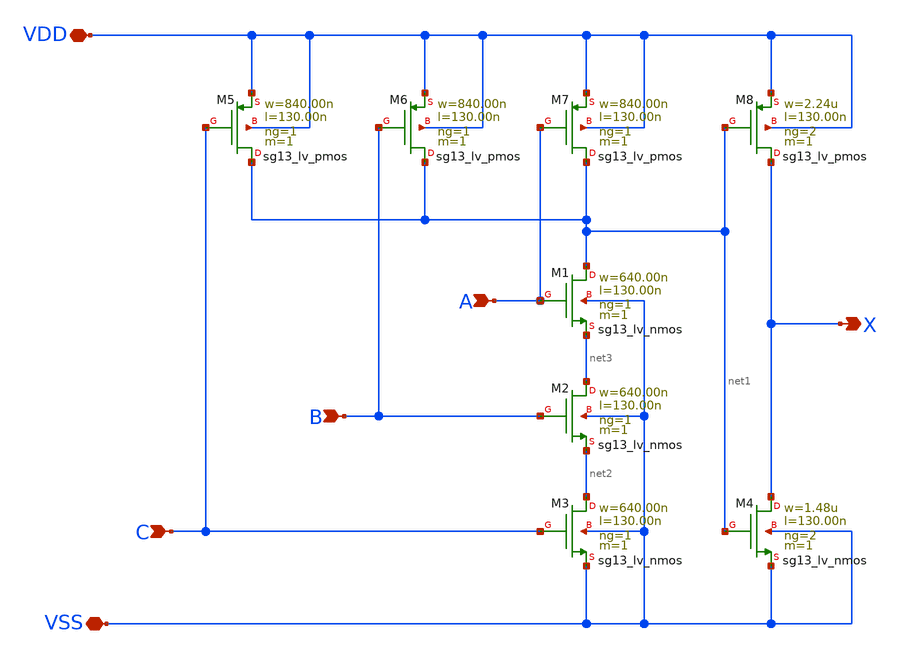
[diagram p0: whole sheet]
** sch_path: ihp-sg13g2/libs.tech/xschem/sg13g2_stdcells/sg13g2_and3_2.sch
* Copyright 2023 IHP PDK Authors
* Licensed under the Apache License, Version 2.0 (the "License");
* you may not use this file except in compliance with the License.
* You may obtain a copy of the License at
* https://www.apache.org/licenses/LICENSE-2.0
* Unless required by applicable law or agreed to in writing, software
* distributed under the License is distributed on an "AS IS" BASIS,
* WITHOUT WARRANTIES OR CONDITIONS OF ANY KIND, either express or implied.
* See the License for the specific language governing permissions and
* limitations under the License.
**.subckt sg13g2_and3_2 X C B A VDD VSS
*.opin X
*.ipin C
*.ipin B
*.ipin A
*.iopin VDD
*.iopin VSS
XM1 net1 A net3 VSS sg13_lv_nmos w=640.00n l=130.00n ng=1 m=1 mm_ok=1
XM2 net3 B net2 VSS sg13_lv_nmos w=640.00n l=130.00n ng=1 m=1 mm_ok=1
XM3 net2 C VSS VSS sg13_lv_nmos w=640.00n l=130.00n ng=1 m=1 mm_ok=1
XM4 X net1 VSS VSS sg13_lv_nmos w=1.48u l=130.00n ng=2 m=1 mm_ok=1
XM5 net1 C VDD VDD sg13_lv_pmos w=840.00n l=130.00n ng=1 m=1 mm_ok=1
XM6 net1 B VDD VDD sg13_lv_pmos w=840.00n l=130.00n ng=1 m=1 mm_ok=1
XM7 net1 A VDD VDD sg13_lv_pmos w=840.00n l=130.00n ng=1 m=1 mm_ok=1
XM8 X net1 VDD VDD sg13_lv_pmos w=2.24u l=130.00n ng=2 m=1 mm_ok=1
**.ends
.end
